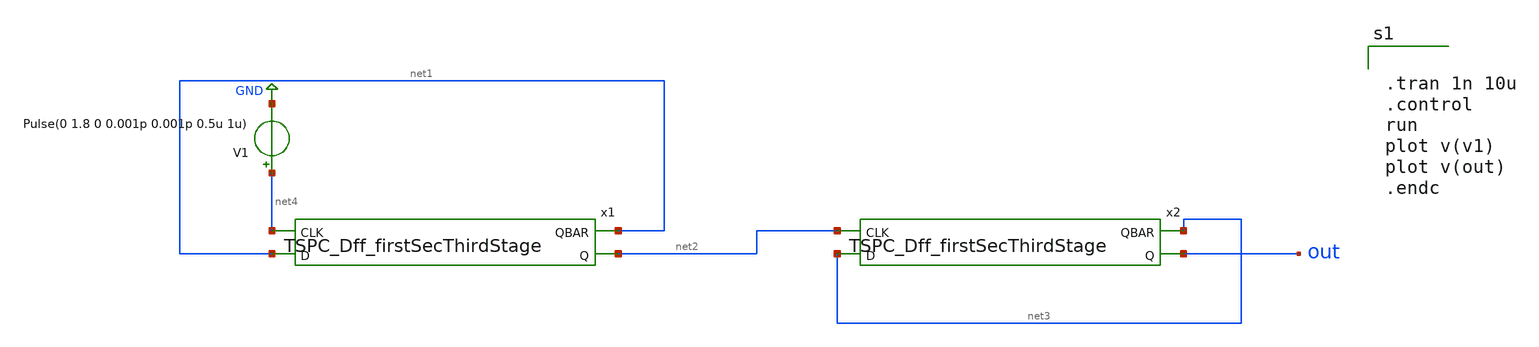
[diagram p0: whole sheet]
** sch_path: untitled-2.sch
**.subckt untitled-2
x1 net1 net2 net4 net1 TSPC_Dff_firstSecThirdStage
x2 net3 out net2 net3 TSPC_Dff_firstSecThirdStage
V1 net4 GND Pulse(0 1.8 0 0.001p 0.001p 0.5u 1u)
**** begin user architecture code


.tran 1n 10u
.control
run
plot v(v1)
plot v(out)
.endc


*.lib ~/open_pdks/sky130/sky130A/libs.tech/ngspice/sky130.lib.spice tt
.param mc_mm_switch=0
.param mc_pr_switch=0

.include ~/open_pdks/sky130/sky130A/libs.tech/ngspice/corners/tt/nonfet.spice


*model
.include ~/open_pdks/sky130/sky130A/libs.tech/ngspice/all.spice

*mosfet
.include ~/open_pdks/sky130/sky130A/libs.ref/sky130_fd_pr/spice/sky130_fd_pr__pfet_01v8__tt.corner.spice
.inclued ~/open_pdks/sky130/sky130A/libs.ref/sky130_fd_pr/spice/sky130_fd_pr__nfet_01v8__tt.corner.spice

*mismatch parameters
.include ~/open_pdks/sky130/sky130A/libs.ref/sky130_fd_pr/spice/sky130_fd_pr__pfet_01v8__mismatch.corner.spice
.include ~/open_pdks/sky130/sky130A/libs.ref/sky130_fd_pr/spice/sky130_fd_pr__nfet_01v8__mismatch.corner.spice

**** end user architecture code
**.ends

* expanding   symbol:  /home/cegrahul/Desktop/TSPC_Dff_firstSecThirdStage.sym # of pins=4
** sym_path: TSPC_Dff_firstSecThirdStage.sym
** sch_path: TSPC_Dff_firstSecThirdStage.sch
.subckt TSPC_Dff_firstSecThirdStage QBAR Q CLK D
*.ipin D
*.ipin CLK
*.opin Q
*.opin QBAR
V1 VDD GND 1.8
XM3 voutfirst D GND GND sky130_fd_pr__nfet_01v8 L=0.15 W=0.36 nf=1 ad='int((nf+1)/2) * W/nf * 0.29' as='int((nf+2)/2) * W/nf * 0.29'
+ pd='2*int((nf+1)/2) * (W/nf + 0.29)' ps='2*int((nf+2)/2) * (W/nf + 0.29)' nrd='0.29 / W' nrs='0.29 / W'
+ sa=0 sb=0 sd=0 mult=1 m=1
XM4 net1 D VDD VDD sky130_fd_pr__pfet_01v8 L=0.15 W=1.68 nf=1 ad='int((nf+1)/2) * W/nf * 0.29' as='int((nf+2)/2) * W/nf * 0.29'
+ pd='2*int((nf+1)/2) * (W/nf + 0.29)' ps='2*int((nf+2)/2) * (W/nf + 0.29)' nrd='0.29 / W' nrs='0.29 / W'
+ sa=0 sb=0 sd=0 mult=1 m=1
XM5 voutfirst CLK net1 VDD sky130_fd_pr__pfet_01v8 L=0.15 W=1.68 nf=1 ad='int((nf+1)/2) * W/nf * 0.29'
+ as='int((nf+2)/2) * W/nf * 0.29' pd='2*int((nf+1)/2) * (W/nf + 0.29)' ps='2*int((nf+2)/2) * (W/nf + 0.29)'
+ nrd='0.29 / W' nrs='0.29 / W' sa=0 sb=0 sd=0 mult=1 m=1
XM1 net2 CLK GND GND sky130_fd_pr__nfet_01v8 L=0.15 W=0.36 nf=1 ad='int((nf+1)/2) * W/nf * 0.29' as='int((nf+2)/2) * W/nf * 0.29'
+ pd='2*int((nf+1)/2) * (W/nf + 0.29)' ps='2*int((nf+2)/2) * (W/nf + 0.29)' nrd='0.29 / W' nrs='0.29 / W'
+ sa=0 sb=0 sd=0 mult=1 m=1
XM2 voutsec CLK VDD VDD sky130_fd_pr__pfet_01v8 L=0.15 W=1.68 nf=1 ad='int((nf+1)/2) * W/nf * 0.29' as='int((nf+2)/2) * W/nf * 0.29'
+ pd='2*int((nf+1)/2) * (W/nf + 0.29)' ps='2*int((nf+2)/2) * (W/nf + 0.29)' nrd='0.29 / W' nrs='0.29 / W'
+ sa=0 sb=0 sd=0 mult=1 m=1
XM6 voutsec voutfirst net2 GND sky130_fd_pr__nfet_01v8 L=0.15 W=0.36 nf=1 ad='int((nf+1)/2) * W/nf * 0.29'
+ as='int((nf+2)/2) * W/nf * 0.29' pd='2*int((nf+1)/2) * (W/nf + 0.29)' ps='2*int((nf+2)/2) * (W/nf + 0.29)'
+ nrd='0.29 / W' nrs='0.29 / W' sa=0 sb=0 sd=0 mult=1 m=1
XM7 net3 voutsec GND GND sky130_fd_pr__nfet_01v8 L=2 W=0.42 nf=1 ad='int((nf+1)/2) * W/nf * 0.29' as='int((nf+2)/2) * W/nf * 0.29'
+ pd='2*int((nf+1)/2) * (W/nf + 0.29)' ps='2*int((nf+2)/2) * (W/nf + 0.29)' nrd='0.29 / W' nrs='0.29 / W'
+ sa=0 sb=0 sd=0 mult=1 m=1
XM8 voutthird voutsec VDD VDD sky130_fd_pr__pfet_01v8 L=0.15 W=1.68 nf=1 ad='int((nf+1)/2) * W/nf * 0.29'
+ as='int((nf+2)/2) * W/nf * 0.29' pd='2*int((nf+1)/2) * (W/nf + 0.29)' ps='2*int((nf+2)/2) * (W/nf + 0.29)'
+ nrd='0.29 / W' nrs='0.29 / W' sa=0 sb=0 sd=0 mult=1 m=1
XM9 voutthird CLK net3 GND sky130_fd_pr__nfet_01v8 L=2 W=0.42 nf=1 ad='int((nf+1)/2) * W/nf * 0.29' as='int((nf+2)/2) * W/nf * 0.29'
+ pd='2*int((nf+1)/2) * (W/nf + 0.29)' ps='2*int((nf+2)/2) * (W/nf + 0.29)' nrd='0.29 / W' nrs='0.29 / W'
+ sa=0 sb=0 sd=0 mult=1 m=1
x1 net4 net5 inverter
x2 net6 net7 inverter
.ends


* expanding   symbol:  /home/cegrahul/Desktop/SSCS/inverter.sym # of pins=2
** sym_path: inverter.sym
** sch_path: inverter.sch
.subckt inverter vin vout
*.ipin vin
*.opin vout
XM2 vout vin net1 net1 sky130_fd_pr__pfet_01v8 L=0.15 W=1.68 nf=1 ad='int((nf+1)/2) * W/nf * 0.29' as='int((nf+2)/2) * W/nf * 0.29'
+ pd='2*int((nf+1)/2) * (W/nf + 0.29)' ps='2*int((nf+2)/2) * (W/nf + 0.29)' nrd='0.29 / W' nrs='0.29 / W'
+ sa=0 sb=0 sd=0 mult=1 m=1
XM3 vout vin GND GND sky130_fd_pr__nfet_01v8 L=0.15 W=0.36 nf=1 ad='int((nf+1)/2) * W/nf * 0.29' as='int((nf+2)/2) * W/nf * 0.29'
+ pd='2*int((nf+1)/2) * (W/nf + 0.29)' ps='2*int((nf+2)/2) * (W/nf + 0.29)' nrd='0.29 / W' nrs='0.29 / W'
+ sa=0 sb=0 sd=0 mult=1 m=1
V3 net1 GND 1.8
.ends

.GLOBAL GND
.end
